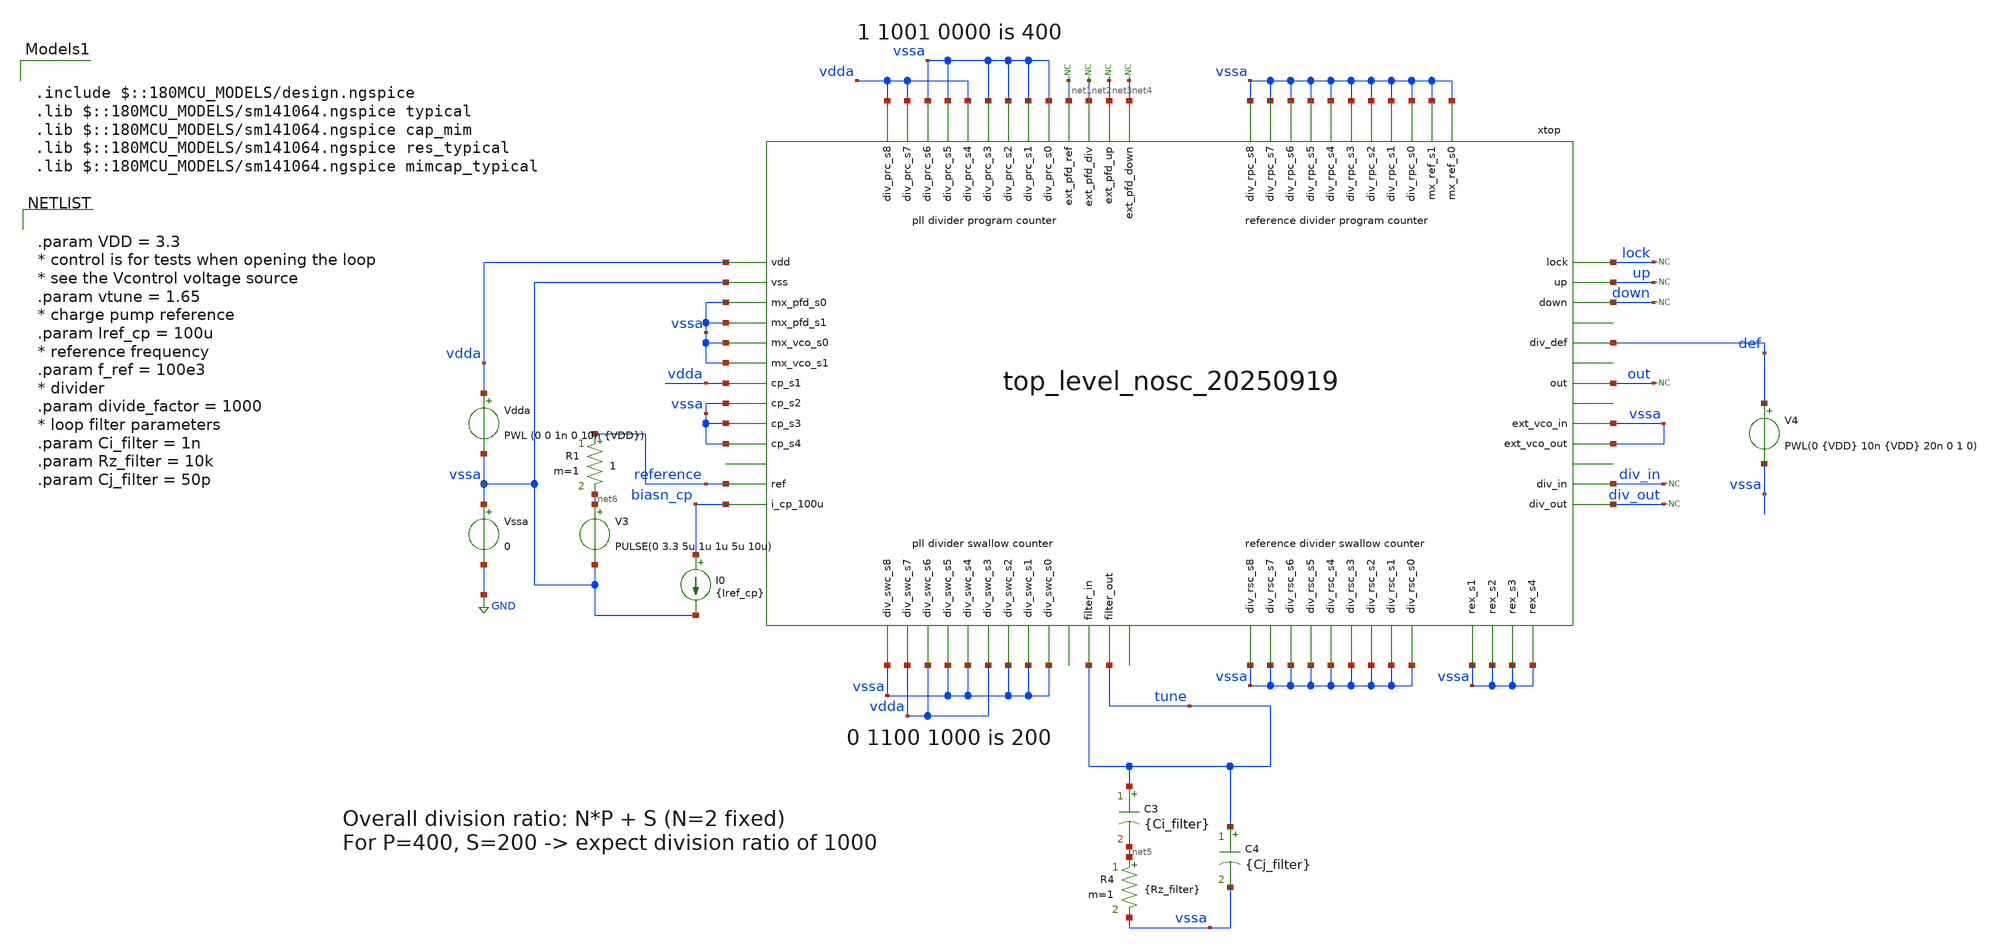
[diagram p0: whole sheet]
** sch_path: designs/libs/tb_top_level/tb_top_level_20250919_nosc.sch
**.subckt tb_top_level_20250919_nosc
Vssa vssa GND 0
Vdda vdda vssa PWL (0 0 1n 0 10n {VDD})
I0 biasn_cp vssa {Iref_cp}
V4 def vssa PWL(0 {VDD} 10n {VDD} 20n 0 1 0)
* noconn #net1
* noconn #net2
* noconn #net3
* noconn #net4
* noconn div_in
* noconn div_out
* noconn down
* noconn up
* noconn lock
C3 tune net5 {Ci_filter} m=1
R4 net5 vssa {Rz_filter} m=1
C4 tune vssa {Cj_filter} m=1
* noconn out
V3 net6 vssa PULSE(0 3.3 5u 1u 1u 5u 10u)
R1 reference net6 1 m=1
xtop vdda vssa vssa vssa vssa vssa vssa vdda vssa vssa vssa vdda vdda vssa vssa vdda vssa vssa vssa
+ vdda vdda vssa vssa vdda vssa vssa vssa vssa reference biasn_cp net1 net2 net3 net4 lock up down tune
+ vssa div_in div_out out tune vssa def vssa vssa vssa vssa vssa vssa vssa vssa vssa vssa vssa vssa vssa
+ vssa vssa vssa vssa vssa vssa vssa vssa vssa vssa vssa top_level_20250919_nosc
**** begin user architecture code


.param VDD = 3.3
* control is for tests when opening the loop
* see the Vcontrol voltage source
.param vtune = 1.65
* charge pump reference
.param Iref_cp = 100u
* reference frequency
.param f_ref = 100e3
* divider
.param divide_factor = 1000
* loop filter parameters
.param Ci_filter = 1n
.param Rz_filter = 10k
.param Cj_filter = 50p



.include $::180MCU_MODELS/design.ngspice
.lib $::180MCU_MODELS/sm141064.ngspice typical
.lib $::180MCU_MODELS/sm141064.ngspice cap_mim
.lib $::180MCU_MODELS/sm141064.ngspice res_typical
.lib $::180MCU_MODELS/sm141064.ngspice mimcap_typical



.save v(tune) v(out) v(reference) v(up) v(down) v(xtop.int_div_out) v(xtop.int_div_in) v(xtop.dff_pfd_ref) v(xtop.dff_pfd_up) v(xtop.up_pre) v(xtop.up_post) v(xtop.down_pre) v(xtop.down_post) v(lock)
.save v(xtop.xpfd.x1.rst) v(xtop.xpfd.x1.net2) v(xtop.xpfd.x1.net3) v(xtop.xpfd.x1.net4) v(xtop.xpfd.x1.net6)
.save v(xtop.xpfd.x1.net5) v(xtop.xpfd.x1.Qb) v(xtop.xpfd.x1.clka) v(xtop.xpfd.x1.clkb)

.control
set filetype=raw
tran 1n 200u
write tb_top_level_sc_20250912.raw
.endc


**** end user architecture code
**.ends
.GLOBAL GND
.end
